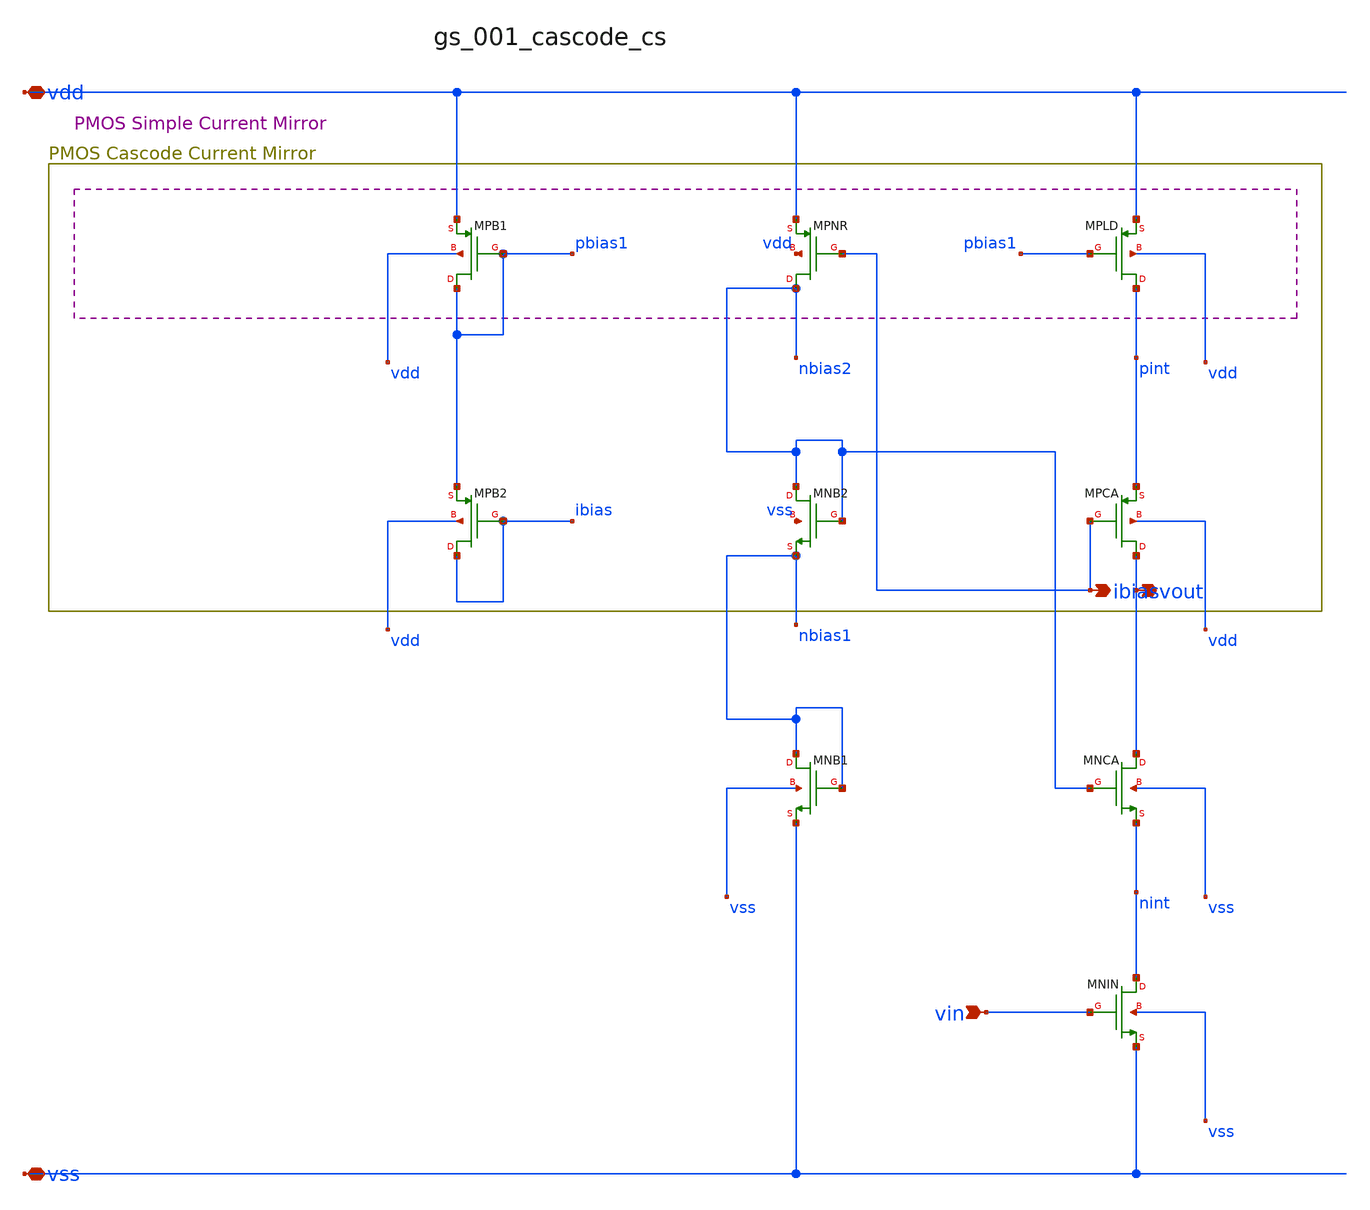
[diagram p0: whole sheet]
** sch_path: analog-db/raw/gs_001_cascode_cs/gs_001_cascode_cs_annotated.sch
**.subckt gs_001_cascode_cs_annotated vin vdd vss ibias vout
*.ipin vin
*.iopin vdd
*.iopin vss
*.opin ibias
*.opin vout
XMNB1 nbias1 nbias1 vss vss sg13_lv_nmos w=x_dut_xmnb1_w l=x_dut_xmnb1_l ng=1 m=x_dut_xmnb1_m
XMNB2 nbias2 nbias2 nbias1 vss sg13_lv_nmos w=x_dut_xmnb2_w l=x_dut_xmnb2_l ng=1 m=x_dut_xmnb2_m
XMNCA vout nbias2 nint vss sg13_lv_nmos w=x_dut_xmnca_w l=x_dut_xmnca_l ng=1 m=x_dut_xmnca_m
XMNIN nint vin vss vss sg13_lv_nmos w=x_dut_xmnin_w l=x_dut_xmnin_l ng=1 m=x_dut_xmnin_m
XMPB1 pbias1 pbias1 vdd vdd sg13_lv_pmos w=x_dut_xmpb1_w l=x_dut_xmpb1_l ng=1 m=x_dut_xmpb1_m
XMPB2 ibias ibias pbias1 vdd sg13_lv_pmos w=x_dut_xmpb2_w l=x_dut_xmpb2_l ng=1 m=x_dut_xmpb2_m
XMPCA vout ibias pint vdd sg13_lv_pmos w=x_dut_xmpca_w l=x_dut_xmpca_l ng=1 m=x_dut_xmpca_m
XMPLD pint pbias1 vdd vdd sg13_lv_pmos w=x_dut_xmpld_w l=x_dut_xmpld_l ng=1 m=x_dut_xmpld_m
XMPNR nbias2 ibias vdd vdd sg13_lv_pmos w=x_dut_xmpnr_w l=x_dut_xmpnr_l ng=1 m=x_dut_xmpnr_m
**.ends
.end
